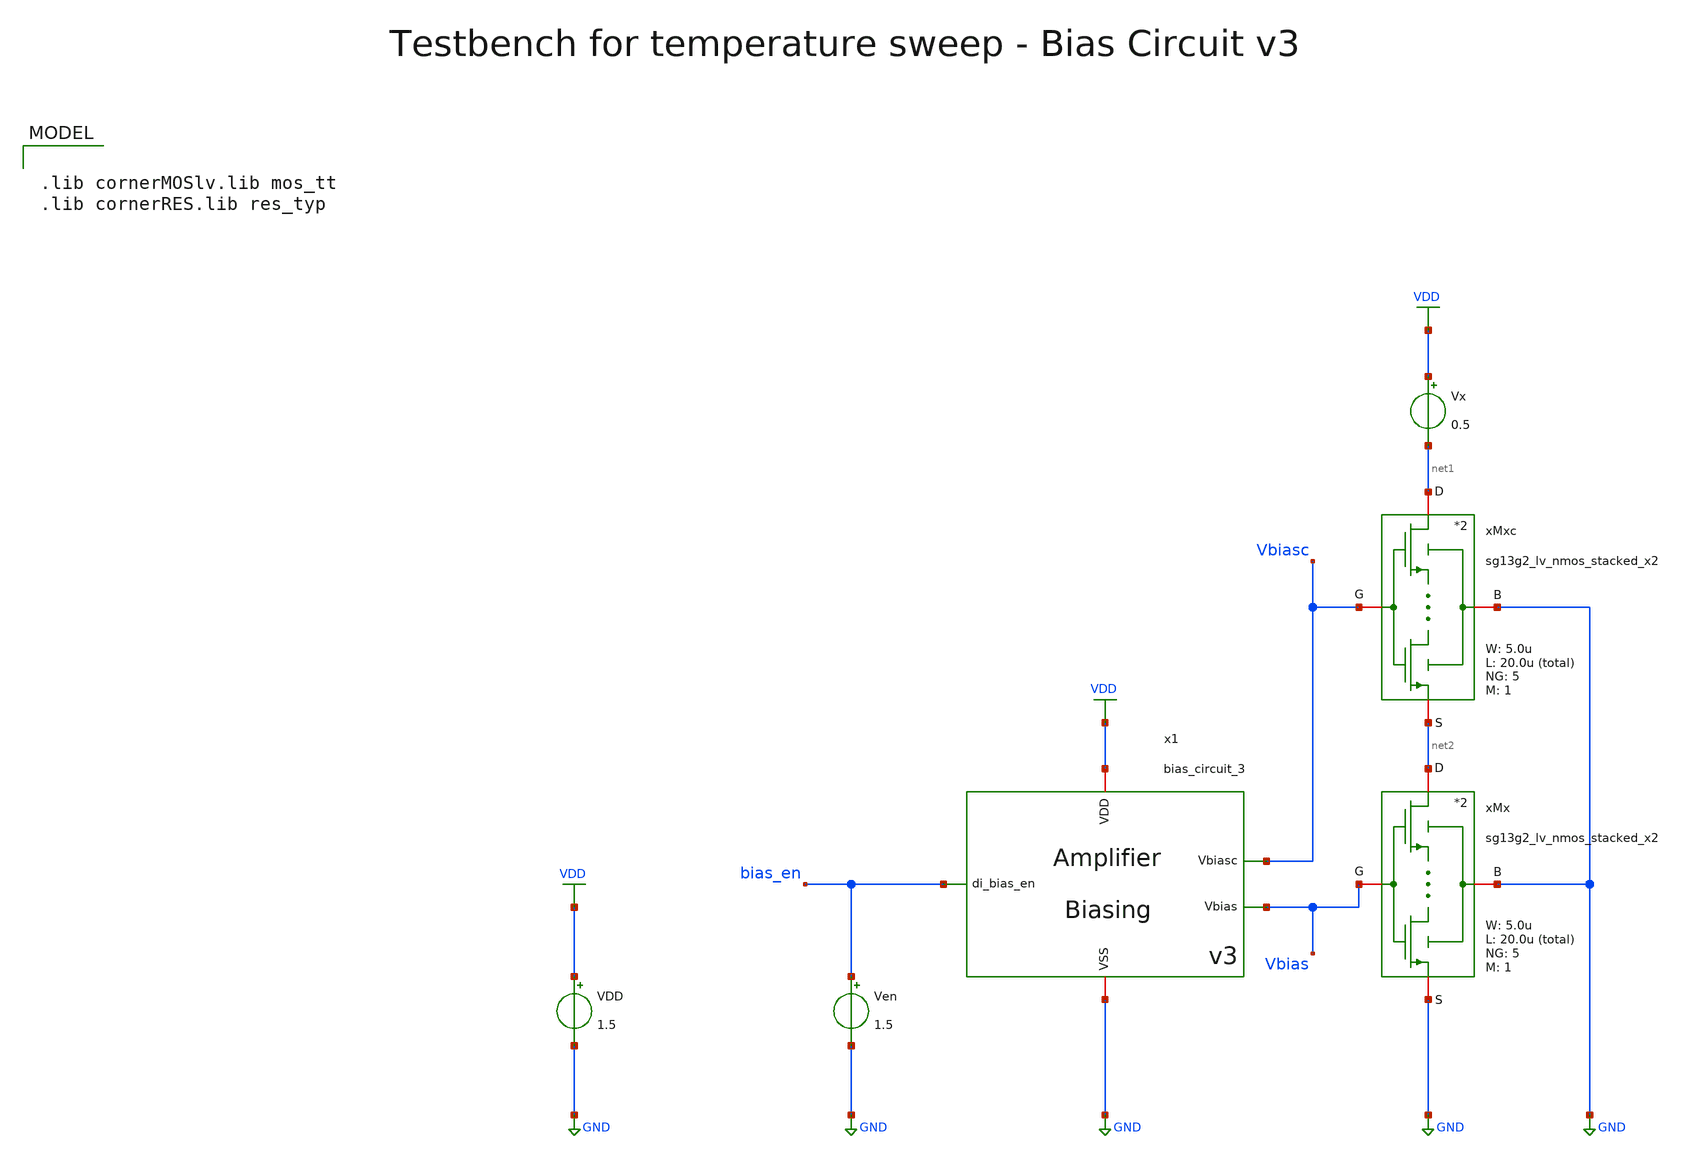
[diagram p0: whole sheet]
** sch_path: SG13G2_ATBS-ADC-main/xschem/bio_amplifier/amplifier_core/bias_circuit/bias_circuit_3/testbenches/bias_circuit_3_tb_temp.sch
**.subckt bias_circuit_3_tb_temp
Ven bias_en GND 1.5
VDD VDD GND 1.5
x1 bias_en VDD GND Vbias Vbiasc bias_circuit_3
Vx VDD net1 0.5
xMx net2 Vbias GND GND sg13g2_lv_nmos_stacked_x2 W_N=5.0u L_N=20.0u NG_N=5 M_N=1
xMxc net1 Vbiasc GND net2 sg13g2_lv_nmos_stacked_x2 W_N=5.0u L_N=20.0u NG_N=5 M_N=1
**** begin user architecture code

.lib cornerMOSlv.lib mos_tt
.lib cornerRES.lib res_typ



.param temp=27
.options savecurrents reltol=1e-3 abstol=1e-15 gmin=1e-15
.control
save all

* User Constants
* Commercial Temperature Range
let Troom = 27
let Tmin = 0
let Tmax = 70
let Tstep = 1

* Operating Point Analysis
op
remzerovec
write bias_circuit_3_tb_temp.raw
set appendwrite

* Temperature Sweep
dc temp $&Tmin $&Tmax $&Tstep
remzerovec
write bias_circuit_3_tb_temp.raw

* Plotting
plot v(Vbias) v(Vbiasc)
plot i(Vx)

* Measurements of Vbias
meas dc Vbias_Troom FIND Vbias at=Troom
meas dc Vbias_Tmin FIND Vbias at=Tmin
meas dc Vbias_Tmax FIND Vbias at=Tmax

* Calculate ppm/°C
let dVbias = Vbias_Tmax - Vbias_Tmin
print dVbias

let dT = Tmax - Tmin
print dT

let ppm_deg = (dVbias / Vbias_Troom) * (1e6 / dT)
print ppm_deg

* Measurements of Ix
meas dc Ix_Troom FIND i(Vx) at=Troom
meas dc Ix_Tmin FIND i(Vx) at=Tmin
meas dc Ix_Tmax FIND i(Vx) at=Tmax

* Calculate ppm/°C
let dIx = Ix_Tmax - Ix_Tmin
print dIx

let ppm_deg = (dIx / Ix_Troom) * (1e6 / dT)
print ppm_deg

* Write Data
set wr_vecnames
set wr_singlescale
let Ix=i(Vx)
wrdata /foss/designs/SG13G2_ATBS-ADC-main/python/plot_simulations/data/bias_circuit_3_tb_temp.txt
+ v(Vbias) v(Ix)

*quit
.endc

**** end user architecture code
**.ends

* expanding   symbol:  bio_amplifier/amplifier_core/bias_circuit/bias_circuit_3/bias_circuit_3.sym #
*+ of pins=5
** sym_path: SG13G2_ATBS-ADC-main/xschem/bio_amplifier/amplifier_core/bias_circuit/bias_circuit_3/bias_circuit_3.sym
** sch_path: SG13G2_ATBS-ADC-main/xschem/bio_amplifier/amplifier_core/bias_circuit/bias_circuit_3/bias_circuit_3.sch
.subckt bias_circuit_3 di_bias_en VDD VSS Vbias Vbiasc
*.iopin VDD
*.iopin VSS
*.opin Vbias
*.ipin di_bias_en
*.opin Vbiasc
XMDEC1 net1 Vbias net1 net1 sg13_lv_nmos w=100.0u l=40.0u ng=100 m=1 mm_ok=1
VIref net4 net7 0
.save i(viref)
VIout net6 Vbiasc 0
.save i(viout)
x1 VDD di_bias_en bias_en_n VSS inverter_lv W_P=1.0u L_P=0.13u W_N=1.0u L_N=0.13u
XMPD1 Vgs_m34 di_bias_en net2 net2 sg13_lv_pmos w=1.0u l=0.13u ng=1 m=1 mm_ok=1
XMPD2 net4 bias_en_n Vgs_m34 net2 sg13_lv_pmos w=1.0u l=0.13u ng=1 m=1 mm_ok=1
VIref5 net1 VSS 0
.save i(viref5)
VIdd VDD net2 0
.save i(vidd)
xM1 net5 net5 VSS net3 sg13g2_lv_nmos_stacked_x2 W_N=20.0u L_N=20.0u NG_N=20 M_N=1
xM1c net7 Vbiasc VSS net5 sg13g2_lv_nmos_stacked_x2 W_N=5.0u L_N=20.0u NG_N=5 M_N=1
xM2 Vbias Vbias VSS VSS sg13g2_lv_nmos_stacked_x2 W_N=5.0u L_N=20.0u NG_N=5 M_N=1
xM2c Vbiasc Vbiasc VSS Vbias sg13g2_lv_nmos_stacked_x2 W_N=5.0u L_N=20.0u NG_N=5 M_N=1
XMDEC2 net2 Vgs_m34 net2 net2 sg13_lv_pmos w=25.0u l=40.0u ng=25 m=1 mm_ok=1
xM3 net4 Vgs_m34 net2 net2 sg13g2_lv_pmos_stacked_x4 W_P=20.0u L_P=40.0u NG_P=20 M_P=1
xM4 net6 Vgs_m34 net2 net2 sg13g2_lv_pmos_stacked_x4 W_P=20.0u L_P=40.0u NG_P=20 M_P=1
x4 di_bias_en Vgs_m34 Vbias net5 VDD VSS aux_ota
R1 net3 VSS 3.521Meg m=1
XMPD3 net5 bias_en_n VSS VSS sg13_lv_nmos w=1.0u l=0.13u ng=1 m=1 mm_ok=1
XMPD4 Vbias bias_en_n VSS VSS sg13_lv_nmos w=1.0u l=0.13u ng=1 m=1 mm_ok=1
xMSU2 Vsu net9 VSS VSS sg13g2_lv_nmos_stacked_x4 W_N=1.0u L_N=40.0u NG_N=1 M_N=1
xMSU1 net8 Vsu VSS net9 sg13g2_lv_nmos_stacked_x4 W_N=1.0u L_N=40.0u NG_N=1 M_N=1
Vmeas1 net4 net8 0
.save i(vmeas1)
Vmeas2 Vbias net9 0
.save i(vmeas2)
CSU1 net10 Vsu 30f m=1
XMPD6 Vsu di_bias_en net10 net10 sg13_lv_pmos w=1.0u l=0.13u ng=1 m=1 mm_ok=1
XMPD7 Vsu bias_en_n VSS VSS sg13_lv_nmos w=1.0u l=0.13u ng=1 m=1 mm_ok=1
XMPD5 net10 bias_en_n net2 net2 sg13_lv_pmos w=1.0u l=0.13u ng=1 m=1 mm_ok=1
.ends


* expanding   symbol:  stacked_transistors/sg13g2_lv_nmos_stacked/sg13g2_lv_nmos_stacked_x2.sym # of
*+ pins=4
** sym_path: SG13G2_ATBS-ADC-main/xschem/stacked_transistors/sg13g2_lv_nmos_stacked/sg13g2_lv_nmos_stacked_x2.sym
** sch_path: SG13G2_ATBS-ADC-main/xschem/stacked_transistors/sg13g2_lv_nmos_stacked/sg13g2_lv_nmos_stacked_x2.sch
.subckt sg13g2_lv_nmos_stacked_x2 D G B S  W_N=1.0u L_N=0.45u NG_N=1 M_N=1
*.iopin D
*.iopin S
*.iopin G
*.iopin B
XM1 net1 G S B sg13_lv_nmos w=W_N l=L_N/2 ng=NG_N m=M_N mm_ok=1
XM2 D G net1 B sg13_lv_nmos w=W_N l=L_N/2 ng=NG_N m=M_N mm_ok=1
.ends


* expanding   symbol:  inverter/inverter_lv.sym # of pins=4
** sym_path: SG13G2_ATBS-ADC-main/xschem/inverter/inverter_lv.sym
** sch_path: SG13G2_ATBS-ADC-main/xschem/inverter/inverter_lv.sch
.subckt inverter_lv VDD vin vout VSS  W_P=3.0u L_P=0.13u W_N=1.0u L_N=0.13u
*.ipin vin
*.iopin VDD
*.iopin VSS
*.opin vout
XM1 vout vin VDD VDD sg13_lv_pmos w=W_P l=L_P ng=1 m=1 mm_ok=1
XM2 vout vin VSS VSS sg13_lv_nmos w=W_N l=L_N ng=1 m=1 mm_ok=1
.ends


* expanding   symbol:  stacked_transistors/sg13g2_lv_pmos_stacked/sg13g2_lv_pmos_stacked_x4.sym # of
*+ pins=4
** sym_path: SG13G2_ATBS-ADC-main/xschem/stacked_transistors/sg13g2_lv_pmos_stacked/sg13g2_lv_pmos_stacked_x4.sym
** sch_path: SG13G2_ATBS-ADC-main/xschem/stacked_transistors/sg13g2_lv_pmos_stacked/sg13g2_lv_pmos_stacked_x4.sch
.subckt sg13g2_lv_pmos_stacked_x4 D G B S  W_P=1.0u L_P=0.45u NG_P=1 M_P=1
*.iopin D
*.iopin S
*.iopin G
*.iopin B
XM1 net1 G S B sg13_lv_pmos w=W_P l=L_P/4 ng=NG_P m=M_P mm_ok=1
XM2 net3 G net1 B sg13_lv_pmos w=W_P l=L_P/4 ng=NG_P m=M_P mm_ok=1
XM3 net2 G net3 B sg13_lv_pmos w=W_P l=L_P/4 ng=NG_P m=M_P mm_ok=1
XM4 D G net2 B sg13_lv_pmos w=W_P l=L_P/4 ng=NG_P m=M_P mm_ok=1
.ends


* expanding   symbol:  bio_amplifier/amplifier_core/bias_circuit/aux_ota/aux_ota.sym # of pins=6
** sym_path: SG13G2_ATBS-ADC-main/xschem/bio_amplifier/amplifier_core/bias_circuit/aux_ota/aux_ota.sym
** sch_path: SG13G2_ATBS-ADC-main/xschem/bio_amplifier/amplifier_core/bias_circuit/aux_ota/aux_ota.sch
.subckt aux_ota di_ota_en vout vinn vinp VDD VSS
*.iopin VDD
*.iopin VSS
*.ipin di_ota_en
*.ipin vinp
*.ipin vinn
*.opin vout
xM3 net1 Vgs_ma34 net2 net2 sg13g2_lv_pmos_stacked_x4 W_P=20.0u L_P=40.0u NG_P=20 M_P=1
xM4 vout Vgs_ma34 net2 net2 sg13g2_lv_pmos_stacked_x4 W_P=20.0u L_P=40.0u NG_P=20 M_P=1
xM1 net1 vinp VSS VSS sg13g2_lv_nmos_stacked_x2 W_N=5.0u L_N=40.0u NG_N=5 M_N=1
VIdd VDD net2 0
.save i(vidd)
xM2 vout vinn VSS VSS sg13g2_lv_nmos_stacked_x2 W_N=5.0u L_N=40.0u NG_N=5 M_N=1
XMPD1 Vgs_ma34 di_ota_en net2 net2 sg13_lv_pmos w=1.0u l=0.13u ng=1 m=1 mm_ok=1
XMPD2 net1 ota_en_n Vgs_ma34 net2 sg13_lv_pmos w=1.0u l=0.13u ng=1 m=1 mm_ok=1
x1 VDD di_ota_en ota_en_n VSS inverter_lv W_P=1.0u L_P=0.13u W_N=1.0u L_N=0.13u
.ends


* expanding   symbol:  stacked_transistors/sg13g2_lv_nmos_stacked/sg13g2_lv_nmos_stacked_x4.sym # of
*+ pins=4
** sym_path: SG13G2_ATBS-ADC-main/xschem/stacked_transistors/sg13g2_lv_nmos_stacked/sg13g2_lv_nmos_stacked_x4.sym
** sch_path: SG13G2_ATBS-ADC-main/xschem/stacked_transistors/sg13g2_lv_nmos_stacked/sg13g2_lv_nmos_stacked_x4.sch
.subckt sg13g2_lv_nmos_stacked_x4 D G B S  W_N=1.0u L_N=0.45u NG_N=1 M_N=1
*.iopin D
*.iopin S
*.iopin G
*.iopin B
XM1 net1 G S B sg13_lv_nmos w=W_N l=L_N/4 ng=NG_N m=M_N mm_ok=1
XM2 net3 G net1 B sg13_lv_nmos w=W_N l=L_N/4 ng=NG_N m=M_N mm_ok=1
XM3 net2 G net3 B sg13_lv_nmos w=W_N l=L_N/4 ng=NG_N m=M_N mm_ok=1
XM4 D G net2 B sg13_lv_nmos w=W_N l=L_N/4 ng=NG_N m=M_N mm_ok=1
.ends

.GLOBAL GND
.GLOBAL VDD
.end
